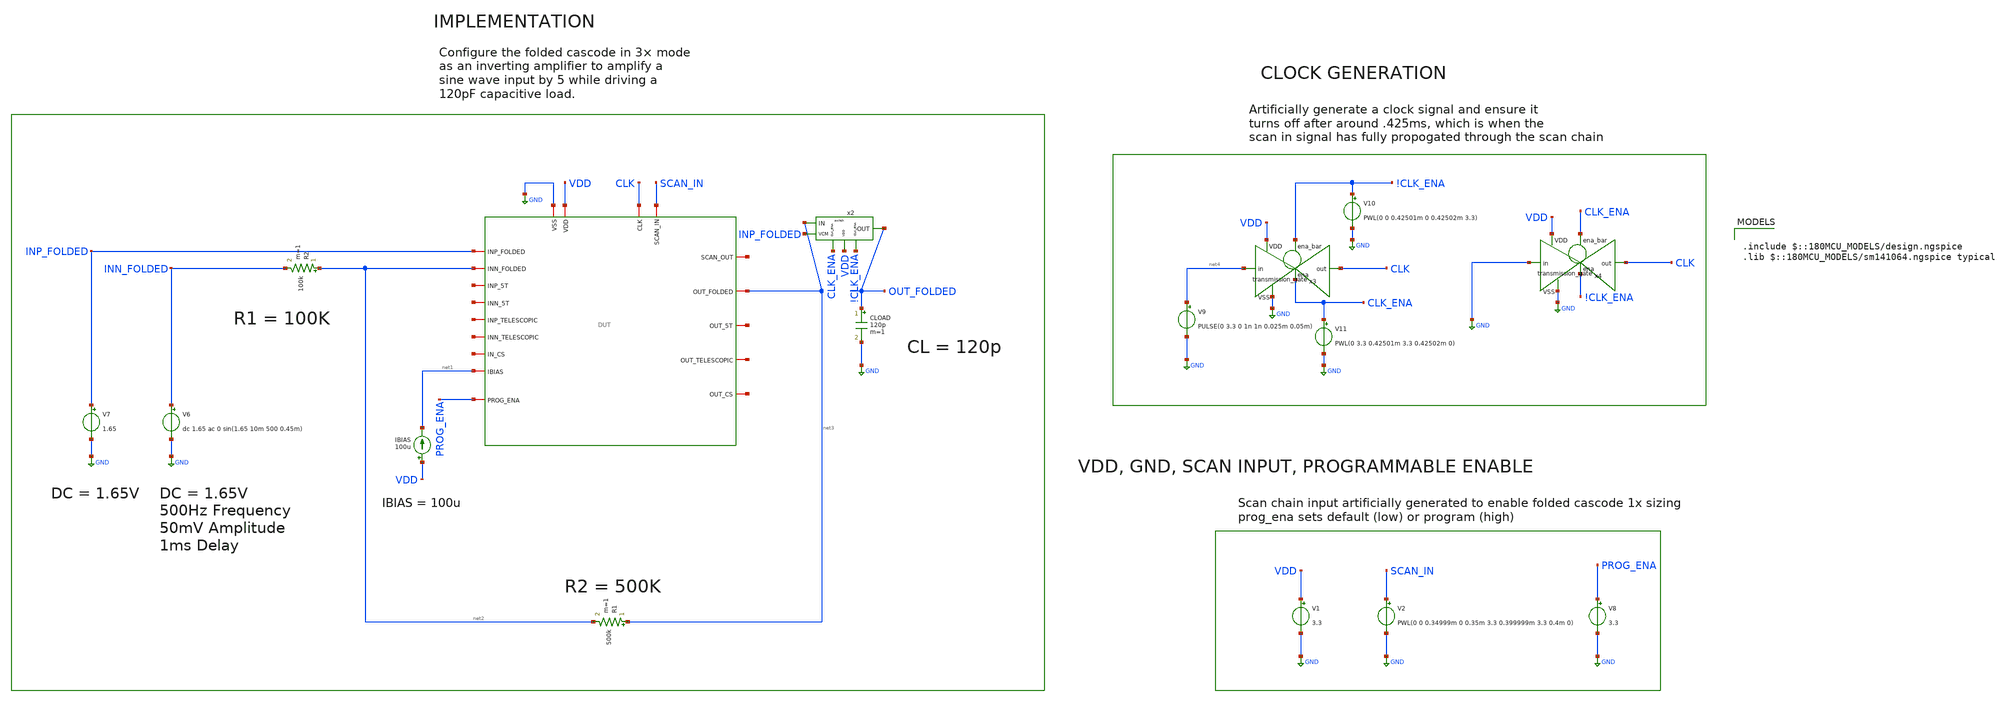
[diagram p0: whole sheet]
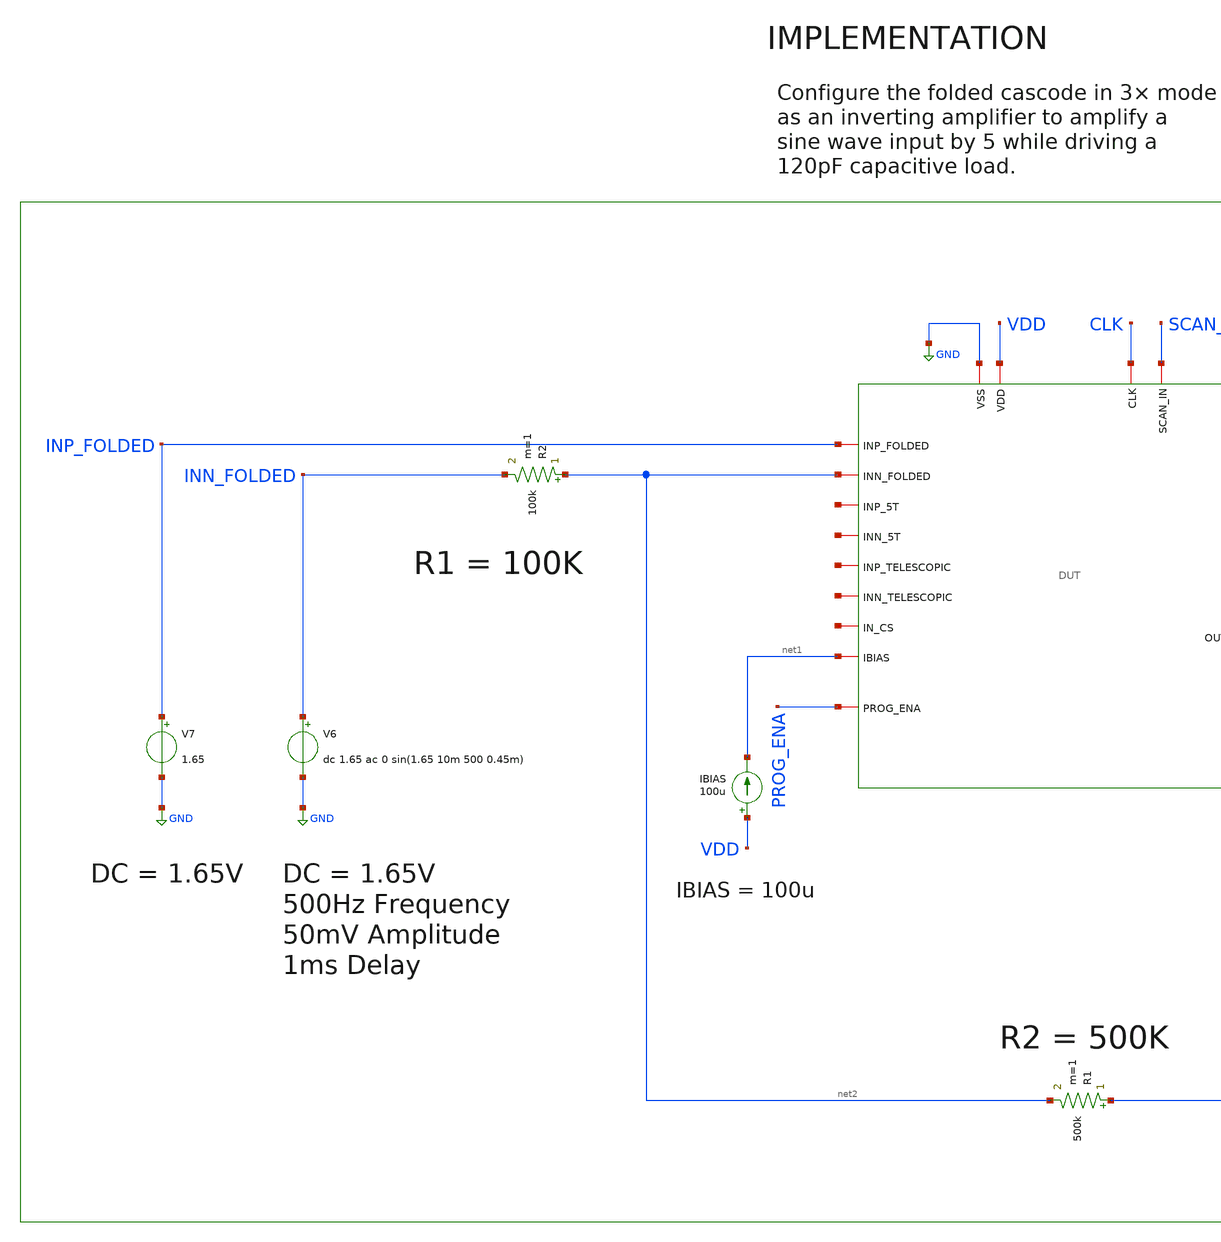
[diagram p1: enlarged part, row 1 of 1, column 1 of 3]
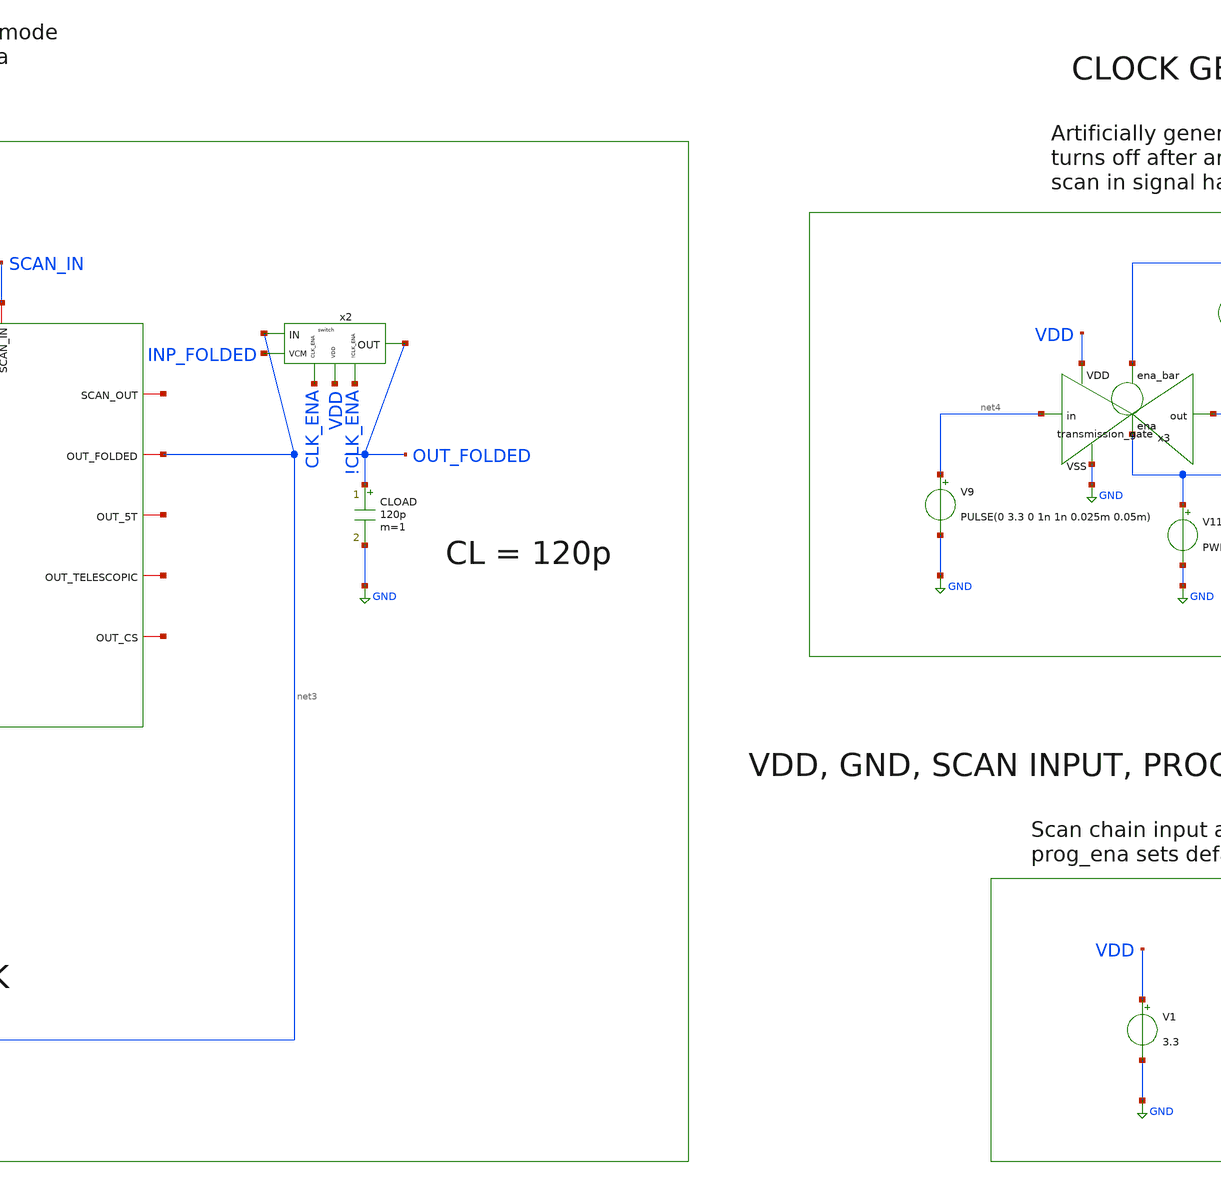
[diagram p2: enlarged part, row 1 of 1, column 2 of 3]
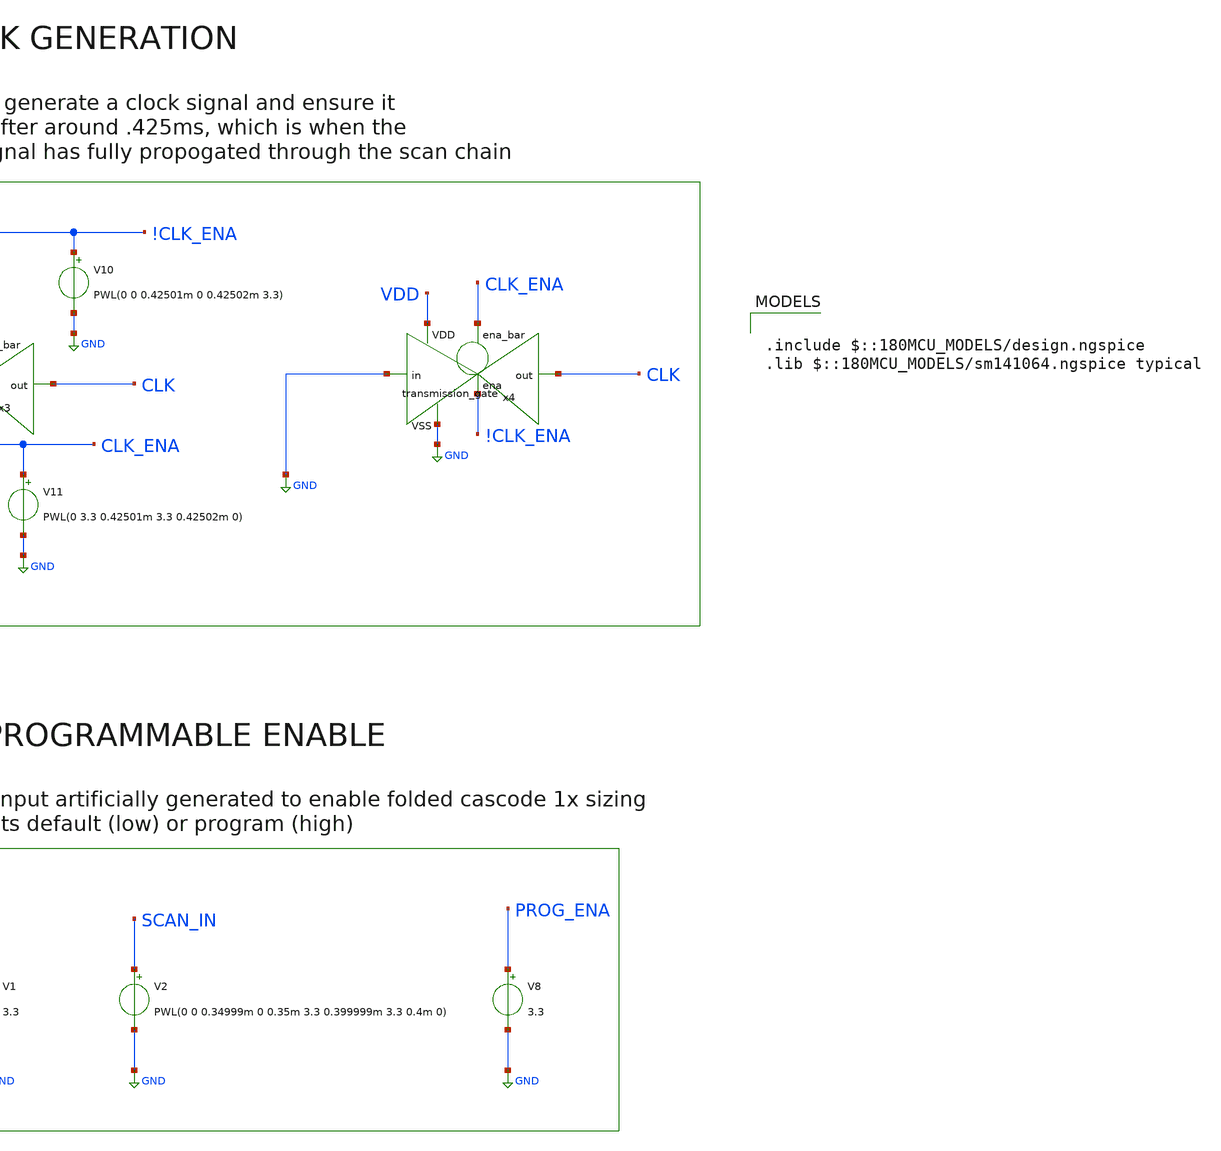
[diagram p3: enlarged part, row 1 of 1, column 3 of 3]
** sch_path: designs/libs/verification/ota_5t/3x_sizing/folded_inverting_amplifier_tb_3x_clean.sch
**.subckt folded_inverting_amplifier_tb_3x_clean
V1 VDD GND 3.3
IBIAS VDD net1 100u
V7 INP_FOLDED GND 1.65
CLOAD OUT_FOLDED GND 120p m=1
R2 net2 INN_FOLDED 100k m=1
V6 INN_FOLDED GND dc 1.65 ac 0 sin(1.65 10m 500 0.45m)
R1 net3 net2 500k m=1
x1 CLK net5 SCAN_IN GND VDD net3 INP_FOLDED net6 net1 net2 net7 net8 net9 net10 net11 net12 net13
+ PROG_ENA DUT
V8 PROG_ENA GND 3.3
V9 net4 GND PULSE(0 3.3 0 1n 1n 0.025m 0.05m)
x3 !CLK_ENA VDD CLK net4 GND CLK_ENA transmission_gate
V10 !CLK_ENA GND PWL(0 0 0.42501m 0 0.42502m 3.3)
V11 CLK_ENA GND PWL(0 3.3 0.42501m 3.3 0.42502m 0)
x4 CLK_ENA VDD CLK GND GND !CLK_ENA transmission_gate
V2 SCAN_IN GND PWL(0 0 0.34999m 0 0.35m 3.3 0.399999m 3.3 0.4m 0)
x2 CLK_ENA VDD !CLK_ENA net3 OUT_FOLDED INP_FOLDED switch
**** begin user architecture code

.include $::180MCU_MODELS/design.ngspice
.lib $::180MCU_MODELS/sm141064.ngspice typical



.control
tran 1u 5m

plot v(out_folded) v(inn_folded)

meas tran vout_pp pp v(out_folded) from=2m to=5m
meas tran vin_pp pp v(inn_folded) from=2m to=5m
let gain = vout_pp / vin_pp
print gain

meas tran vout_dc avg v(out_folded) from=2m to=5m
meas tran vin_dc avg v(inn_folded) from=2m to=5m
let dc_offset = vout_dc - vin_dc
let input_offset = dc_offset / 6
print vout_dc vin_dc dc_offset input_offset

let ideal_gain = 5
let gain_error_pct = (ideal_gain - gain) / ideal_gain * 100
print gain_error_pct

meas tran idd avg i(v1) from=2m to=5m
let power = abs(idd) * 3.3
print idd power
.endc


**** end user architecture code
**.ends
.GLOBAL GND
.end
